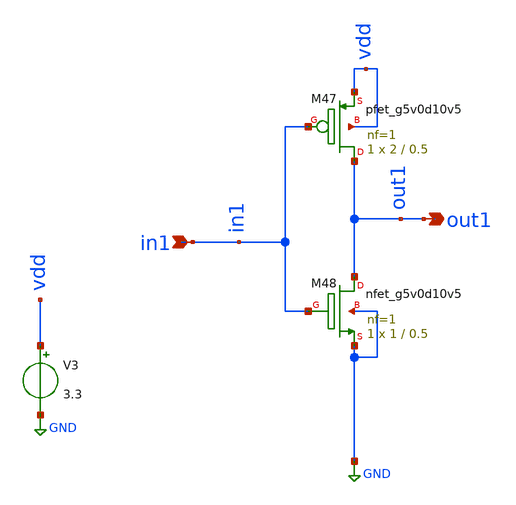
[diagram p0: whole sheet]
** sch_path: xschem/FDC/inverter.sch
**.subckt inverter in1 out1
*.ipin in1
*.opin out1
XM47 out1 in1 vdd vdd sky130_fd_pr__pfet_g5v0d10v5 L=0.5 W=2 nf=1 ad='int((nf+1)/2) * W/nf * 0.29' as='int((nf+2)/2) * W/nf * 0.29'
+ pd='2*int((nf+1)/2) * (W/nf + 0.29)' ps='2*int((nf+2)/2) * (W/nf + 0.29)' nrd='0.29 / W' nrs='0.29 / W'
+ sa=0 sb=0 sd=0 mult=1 m=1
XM48 out1 in1 GND GND sky130_fd_pr__nfet_g5v0d10v5 L=0.5 W=1 nf=1 ad='int((nf+1)/2) * W/nf * 0.29' as='int((nf+2)/2) * W/nf * 0.29'
+ pd='2*int((nf+1)/2) * (W/nf + 0.29)' ps='2*int((nf+2)/2) * (W/nf + 0.29)' nrd='0.29 / W' nrs='0.29 / W'
+ sa=0 sb=0 sd=0 mult=1 m=1
V3 vdd GND 3.3
**.ends
.GLOBAL GND
.end
